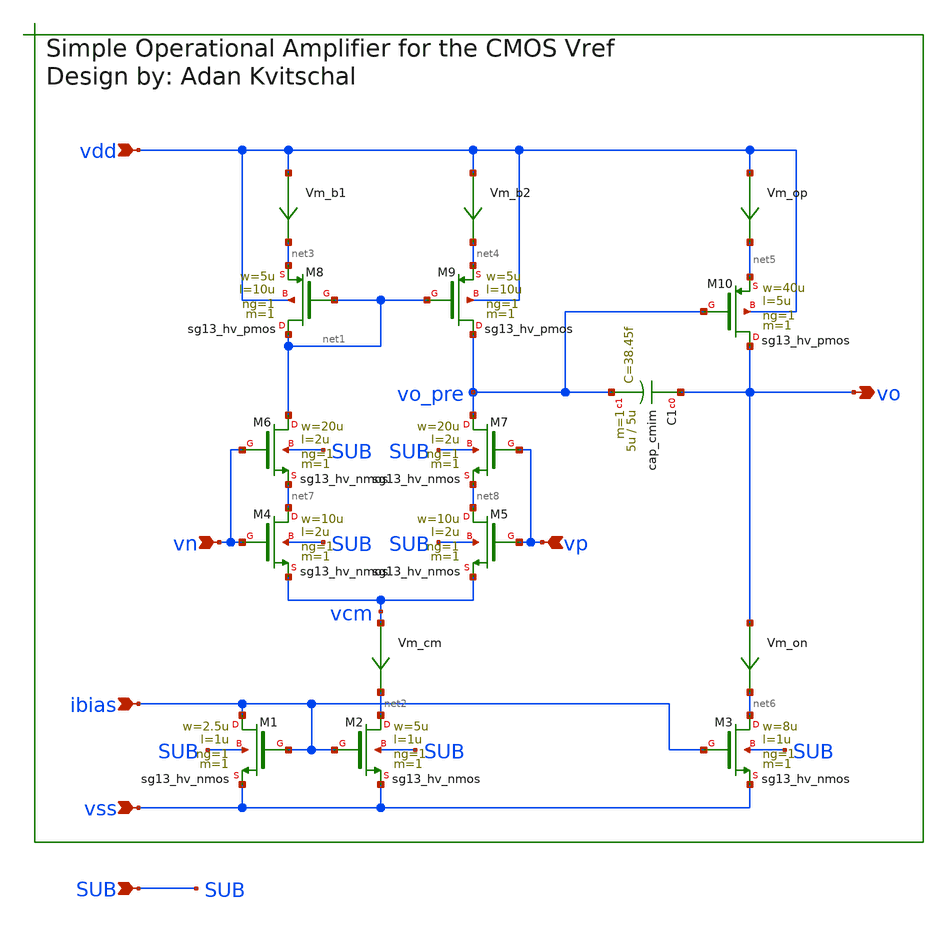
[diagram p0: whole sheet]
** sch_path: release/xschem/sch/output_amp.sch
**.subckt output_amp vp vn ibias vo vss vdd SUB
*.ipin vp
*.ipin vn
*.ipin ibias
*.opin vo
*.ipin vss
*.ipin vdd
*.ipin SUB
Vm_b1 vdd net3 0
.save i(vm_b1)
Vm_op vdd net5 0
.save i(vm_op)
Vm_cm vcm net2 0
.save i(vm_cm)
Vm_b2 vdd net4 0
.save i(vm_b2)
Vm_on vo net6 0
.save i(vm_on)
XM1 ibias ibias vss SUB sg13_hv_nmos w=2.5u l=1u ng=1 m=1 mm_ok=1
XM2 net2 ibias vss SUB sg13_hv_nmos w=5u l=1u ng=1 m=1 mm_ok=1
XM3 net6 ibias vss SUB sg13_hv_nmos w=8u l=1u ng=1 m=1 mm_ok=1
XM4 net7 vn vcm SUB sg13_hv_nmos w=10u l=2u ng=1 m=1 mm_ok=1
XM5 net8 vp vcm SUB sg13_hv_nmos w=10u l=2u ng=1 m=1 mm_ok=1
XC1 vo vo_pre cap_cmim w=5u l=5u m=1 mm_ok=1
XM6 net1 vn net7 SUB sg13_hv_nmos w=20u l=2u ng=1 m=1 mm_ok=1
XM7 vo_pre vp net8 SUB sg13_hv_nmos w=20u l=2u ng=1 m=1 mm_ok=1
XM8 net1 net1 net3 vdd sg13_hv_pmos w=5u l=10u ng=1 m=1 mm_ok=1
XM9 vo_pre net1 net4 vdd sg13_hv_pmos w=5u l=10u ng=1 m=1 mm_ok=1
XM10 vo vo_pre net5 vdd sg13_hv_pmos w=40u l=5u ng=1 m=1 mm_ok=1
**.ends
.end
